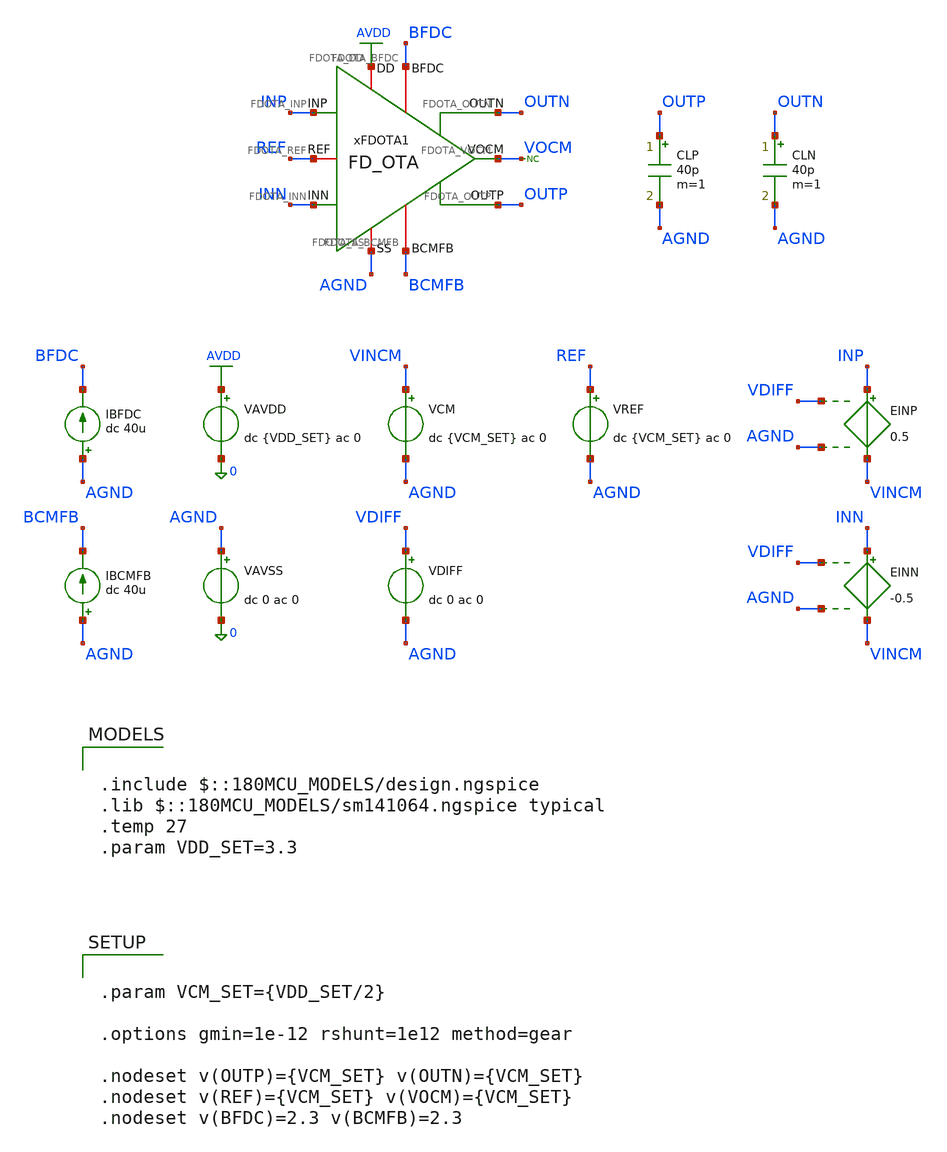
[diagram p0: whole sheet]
** sch_path: Design_Files/IC Design/Testbench/FD_OTA/FDOTA/Open_Loop/FD_OTA_TB_OL_NOM.sch
**.subckt FD_OTA_TB_OL_NOM
IBFDC AGND BFDC dc 40u
VAVDD AVDD 0 dc {VDD_SET} ac 0
.save i(vavdd)
VCM VINCM AGND dc {VCM_SET} ac 0
VDIFF VDIFF AGND dc 0 ac 0
VAVSS AGND 0 dc 0 ac 0
.save i(vavss)
VREF REF AGND dc {VCM_SET} ac 0
EINP INP VINCM VDIFF AGND 0.5
EINN INN VINCM VDIFF AGND -0.5
IBCMFB AGND BCMFB dc 40u
CLP OUTP AGND 40p m=1
CLN OUTN AGND 40p m=1
* noconn VOCM
xFDOTA1 AVDD AGND INP INN OUTN BFDC OUTP BCMFB REF VOCM FD_OTA
**** begin user architecture code

.include $::180MCU_MODELS/design.ngspice
.lib $::180MCU_MODELS/sm141064.ngspice typical
.temp 27
.param VDD_SET=3.3




.control
destroy all
save all
set wr_vecnames
set wr_singlescale
option numdgt=15

shell mkdir -p
+ /foss/designs/ECG_Acquisition_IC/Measurement_Results/IC_Simulation/FD_OTA/FDOTA/NOM.Result_txt

shell rm -f
+ /foss/designs/ECG_Acquisition_IC/Measurement_Results/IC_Simulation/FD_OTA/FDOTA/NOM.Result_txt/NOM.ol_op.txt
shell rm -f
+ /foss/designs/ECG_Acquisition_IC/Measurement_Results/IC_Simulation/FD_OTA/FDOTA/NOM.Result_txt/NOM.ol_diff_ac.txt
shell rm -f
+ /foss/designs/ECG_Acquisition_IC/Measurement_Results/IC_Simulation/FD_OTA/FDOTA/NOM.Result_txt/NOM.ol_cm_ac.txt
shell rm -f
+ /foss/designs/ECG_Acquisition_IC/Measurement_Results/IC_Simulation/FD_OTA/FDOTA/NOM.Result_txt/NOM.ol_psrrp_ac.txt
shell rm -f
+ /foss/designs/ECG_Acquisition_IC/Measurement_Results/IC_Simulation/FD_OTA/FDOTA/NOM.Result_txt/NOM.ol_psrrn_ac.txt
shell rm -f
+ /foss/designs/ECG_Acquisition_IC/Measurement_Results/IC_Simulation/FD_OTA/FDOTA/NOM.Result_txt/NOM.ol_vtc.txt

* OP
op

let voutcm = 0.5*(v(OUTP)+v(OUTN))
let voutdiff = v(OUTP)-v(OUTN)
let idd = -vavdd#branch
let ibias_fdc = 40u + 0*v(AVDD)
let ibias_cmfb = 40u + 0*v(AVDD)

wrdata
+ /foss/designs/ECG_Acquisition_IC/Measurement_Results/IC_Simulation/FD_OTA/FDOTA/NOM.Result_txt/NOM.ol_op.txt v(AVDD) v(INP) v(INN) v(OUTP) v(OUTN) voutcm voutdiff v(REF) v(VOCM) v(BFDC) v(BCMFB) idd ibias_fdc
+ ibias_cmfb

* Diff AC
alter @VCM[ACMAG] = 0
alter @VDIFF[ACMAG] = 1
alter @VDIFF[ACPHASE] = 0
alter @VREF[ACMAG] = 0
alter @VAVDD[ACMAG] = 0
alter @VAVSS[ACMAG] = 0

ac dec 200 0.01 100G

let vin_diff = v(INP)-v(INN)
let voutdiff = v(OUTP)-v(OUTN)
let vin_diff_real = real(vin_diff)
let vin_diff_imag = imag(vin_diff)
let voutdiff_real = real(voutdiff)
let voutdiff_imag = imag(voutdiff)

setscale frequency

wrdata
+ /foss/designs/ECG_Acquisition_IC/Measurement_Results/IC_Simulation/FD_OTA/FDOTA/NOM.Result_txt/NOM.ol_diff_ac.txt vin_diff_real vin_diff_imag voutdiff_real voutdiff_imag

* CM AC
alter @VCM[ACMAG] = 1
alter @VCM[ACPHASE] = 0
alter @VDIFF[ACMAG] = 0
alter @VREF[ACMAG] = 0
alter @VAVDD[ACMAG] = 0
alter @VAVSS[ACMAG] = 0

ac dec 200 0.01 100G

let vin_cm = 0.5*(v(INP)+v(INN))
let voutdiff = v(OUTP)-v(OUTN)
let vin_cm_real = real(vin_cm)
let vin_cm_imag = imag(vin_cm)
let voutdiff_real = real(voutdiff)
let voutdiff_imag = imag(voutdiff)

setscale frequency

wrdata
+ /foss/designs/ECG_Acquisition_IC/Measurement_Results/IC_Simulation/FD_OTA/FDOTA/NOM.Result_txt/NOM.ol_cm_ac.txt vin_cm_real vin_cm_imag voutdiff_real voutdiff_imag

* PSRR+
alter @VCM[ACMAG] = 0
alter @VDIFF[ACMAG] = 0
alter @VREF[ACMAG] = 0
alter @VAVDD[ACMAG] = 1
alter @VAVDD[ACPHASE] = 0
alter @VAVSS[ACMAG] = 0

ac dec 200 0.01 100G

let vavdd_ac = v(AVDD)
let voutdiff = v(OUTP)-v(OUTN)
let vavdd_real = real(vavdd_ac)
let vavdd_imag = imag(vavdd_ac)
let voutdiff_real = real(voutdiff)
let voutdiff_imag = imag(voutdiff)

setscale frequency

wrdata
+ /foss/designs/ECG_Acquisition_IC/Measurement_Results/IC_Simulation/FD_OTA/FDOTA/NOM.Result_txt/NOM.ol_psrrp_ac.txt vavdd_real vavdd_imag voutdiff_real voutdiff_imag

* PSRR-
alter @VCM[ACMAG] = 0
alter @VDIFF[ACMAG] = 0
alter @VREF[ACMAG] = 0
alter @VAVDD[ACMAG] = 0
alter @VAVSS[ACMAG] = 1
alter @VAVSS[ACPHASE] = 0

ac dec 200 0.01 100G

let vagnd_ac = v(AGND)
let voutdiff = v(OUTP)-v(OUTN)
let vagnd_real = real(vagnd_ac)
let vagnd_imag = imag(vagnd_ac)
let voutdiff_real = real(voutdiff)
let voutdiff_imag = imag(voutdiff)

setscale frequency

wrdata
+ /foss/designs/ECG_Acquisition_IC/Measurement_Results/IC_Simulation/FD_OTA/FDOTA/NOM.Result_txt/NOM.ol_psrrn_ac.txt vagnd_real vagnd_imag voutdiff_real voutdiff_imag

* VTC
alter @VCM[ACMAG] = 0
alter @VDIFF[ACMAG] = 0
alter @VREF[ACMAG] = 0
alter @VAVDD[ACMAG] = 0
alter @VAVSS[ACMAG] = 0

dc VDIFF -20m 20m 10u

let vin_diff = v(INP)-v(INN)
let voutcm = 0.5*(v(OUTP)+v(OUTN))
let voutdiff = v(OUTP)-v(OUTN)
let idd = -vavdd#branch

setscale vin_diff

wrdata
+ /foss/designs/ECG_Acquisition_IC/Measurement_Results/IC_Simulation/FD_OTA/FDOTA/NOM.Result_txt/NOM.ol_vtc.txt v(INP) v(INN) v(OUTP) v(OUTN) voutcm voutdiff v(VOCM) idd

quit
.endc




.param VCM_SET={VDD_SET/2}

.options gmin=1e-12 rshunt=1e12 method=gear

.nodeset v(OUTP)={VCM_SET} v(OUTN)={VCM_SET}
.nodeset v(REF)={VCM_SET} v(VOCM)={VCM_SET}
.nodeset v(BFDC)=2.3 v(BCMFB)=2.3


**** end user architecture code
**.ends

* expanding   symbol:  ECG_Acquisition_IC/Design_Files/IC Design/Schematic/FD_OTA/FDOTA/FD_OTA.sym #
*+ of pins=10
** sym_path: Design_Files/IC Design/Schematic/FD_OTA/FDOTA/FD_OTA.sym
** sch_path: Design_Files/IC Design/Schematic/FD_OTA/FDOTA/FD_OTA.sch
.subckt FD_OTA FDOTA_DD FDOTA_SS FDOTA_INP FDOTA_INN FDOTA_OUTN FDOTA_BFDC FDOTA_OUTP FDOTA_BCMFB
+ FDOTA_REF FDOTA_VOCM
*.iopin FDOTA_DD
*.iopin FDOTA_SS
*.ipin FDOTA_INP
*.ipin FDOTA_INN
*.opin FDOTA_OUTP
*.iopin FDOTA_BFDC
*.opin FDOTA_OUTN
*.iopin FDOTA_BCMFB
*.iopin FDOTA_REF
*.iopin FDOTA_VOCM
R1 FDOTA_OUTP FDOTA_VOCM 100k m=1
R2 FDOTA_VOCM FDOTA_OUTN 100k m=1
C1 FDOTA_OUTP FDOTA_VOCM 50f m=1
C2 FDOTA_VOCM FDOTA_OUTN 50f m=1
xFDC1 FDOTA_DD FDOTA_SS FDOTA_INP FDOTA_INN FDOTA_OUTN FDOTA_BFDC FDOTA_OUTP FDOTA_VCMFB FDC
xCMFB1 FDOTA_DD FDOTA_SS FDOTA_VOCM FDOTA_REF FDOTA_VCMFB FDOTA_BCMFB CMFB
.ends


* expanding   symbol:  ECG_Acquisition_IC/Design_Files/IC Design/Schematic/FD_OTA/FDC/FDC.sym # of
*+ pins=8
** sym_path: Design_Files/IC Design/Schematic/FD_OTA/FDC/FDC.sym
** sch_path: Design_Files/IC Design/Schematic/FD_OTA/FDC/FDC.sch
.subckt FDC FDC_DD FDC_SS FDC_INP FDC_INN FDC_OUTN FDC_B FDC_OUTP FDC_CMFB
*.iopin FDC_DD
*.iopin FDC_SS
*.ipin FDC_INP
*.ipin FDC_INN
*.opin FDC_OUTP
*.iopin FDC_B
*.opin FDC_OUTN
*.iopin FDC_CMFB
XM3 net4 FDC_CMFB FDC_DD FDC_DD pfet_03v3 L=2u W=1u nf=1 ad='int((nf+1)/2) * W/nf * 0.18u' as='int((nf+2)/2) * W/nf * 0.18u'
+ pd='2*int((nf+1)/2) * (W/nf + 0.18u)' ps='2*int((nf+2)/2) * (W/nf + 0.18u)' nrd='0.18u / W' nrs='0.18u / W'
+ sa=0 sb=0 sd=0 m=200
XM8 FDC_OUTP FDC_B FDC_SS FDC_SS nfet_03v3 L=1u W=1u nf=1 ad='int((nf+1)/2) * W/nf * 0.18u' as='int((nf+2)/2) * W/nf * 0.18u'
+ pd='2*int((nf+1)/2) * (W/nf + 0.18u)' ps='2*int((nf+2)/2) * (W/nf + 0.18u)' nrd='0.18u / W' nrs='0.18u / W'
+ sa=0 sb=0 sd=0 m=200
Rz net1 net2 6k m=1
XM5 net3 FDC_B FDC_SS FDC_SS nfet_03v3 L=2u W=1u nf=1 ad='int((nf+1)/2) * W/nf * 0.18u' as='int((nf+2)/2) * W/nf * 0.18u'
+ pd='2*int((nf+1)/2) * (W/nf + 0.18u)' ps='2*int((nf+2)/2) * (W/nf + 0.18u)' nrd='0.18u / W' nrs='0.18u / W'
+ sa=0 sb=0 sd=0 m=10
XM6 FDC_OUTP net1 FDC_DD FDC_DD pfet_03v3 L=1u W=1u nf=1 ad='int((nf+1)/2) * W/nf * 0.18u' as='int((nf+2)/2) * W/nf * 0.18u'
+ pd='2*int((nf+1)/2) * (W/nf + 0.18u)' ps='2*int((nf+2)/2) * (W/nf + 0.18u)' nrd='0.18u / W' nrs='0.18u / W'
+ sa=0 sb=0 sd=0 m=200
XM10 FDC_B FDC_B FDC_SS FDC_SS nfet_03v3 L=2u W=1u nf=1 ad='int((nf+1)/2) * W/nf * 0.18u' as='int((nf+2)/2) * W/nf * 0.18u'
+ pd='2*int((nf+1)/2) * (W/nf + 0.18u)' ps='2*int((nf+2)/2) * (W/nf + 0.18u)' nrd='0.18u / W' nrs='0.18u / W'
+ sa=0 sb=0 sd=0 m=20
Cc net2 FDC_OUTP 3p m=1
XM9 FDC_OUTN FDC_B FDC_SS FDC_SS nfet_03v3 L=1u W=1u nf=1 ad='int((nf+1)/2) * W/nf * 0.18u' as='int((nf+2)/2) * W/nf * 0.18u'
+ pd='2*int((nf+1)/2) * (W/nf + 0.18u)' ps='2*int((nf+2)/2) * (W/nf + 0.18u)' nrd='0.18u / W' nrs='0.18u / W'
+ sa=0 sb=0 sd=0 m=200
Rz1 net4 net5 6k m=1
XM7 FDC_OUTN net4 FDC_DD FDC_DD pfet_03v3 L=1u W=1u nf=1 ad='int((nf+1)/2) * W/nf * 0.18u' as='int((nf+2)/2) * W/nf * 0.18u'
+ pd='2*int((nf+1)/2) * (W/nf + 0.18u)' ps='2*int((nf+2)/2) * (W/nf + 0.18u)' nrd='0.18u / W' nrs='0.18u / W'
+ sa=0 sb=0 sd=0 m=200
Cc1 net5 FDC_OUTN 3p m=1
XM4 net1 FDC_CMFB FDC_DD FDC_DD pfet_03v3 L=2u W=1u nf=1 ad='int((nf+1)/2) * W/nf * 0.18u' as='int((nf+2)/2) * W/nf * 0.18u'
+ pd='2*int((nf+1)/2) * (W/nf + 0.18u)' ps='2*int((nf+2)/2) * (W/nf + 0.18u)' nrd='0.18u / W' nrs='0.18u / W'
+ sa=0 sb=0 sd=0 m=200
XM1 net4 FDC_INN net3 FDC_SS nfet_03v3 L=2u W=1u nf=1 ad='int((nf+1)/2) * W/nf * 0.18u' as='int((nf+2)/2) * W/nf * 0.18u'
+ pd='2*int((nf+1)/2) * (W/nf + 0.18u)' ps='2*int((nf+2)/2) * (W/nf + 0.18u)' nrd='0.18u / W' nrs='0.18u / W'
+ sa=0 sb=0 sd=0 m=200
XM2 net1 FDC_INP net3 FDC_SS nfet_03v3 L=2u W=1u nf=1 ad='int((nf+1)/2) * W/nf * 0.18u' as='int((nf+2)/2) * W/nf * 0.18u'
+ pd='2*int((nf+1)/2) * (W/nf + 0.18u)' ps='2*int((nf+2)/2) * (W/nf + 0.18u)' nrd='0.18u / W' nrs='0.18u / W'
+ sa=0 sb=0 sd=0 m=200
.ends


* expanding   symbol:  ECG_Acquisition_IC/Design_Files/IC Design/Schematic/FD_OTA/CMFB/CMFB.sym # of
*+ pins=6
** sym_path: Design_Files/IC Design/Schematic/FD_OTA/CMFB/CMFB.sym
** sch_path: Design_Files/IC Design/Schematic/FD_OTA/CMFB/CMFB.sch
.subckt CMFB CMFB_DD CMFB_SS CMFB_IN CMFB_REF CMFB_OUT CMFB_B
*.iopin CMFB_DD
*.iopin CMFB_SS
*.ipin CMFB_IN
*.ipin CMFB_REF
*.opin CMFB_OUT
*.iopin CMFB_B
XM4 CMFB_OUT CMFB_OUT CMFB_DD CMFB_DD pfet_03v3 L=1u W=1u nf=1 ad='int((nf+1)/2) * W/nf * 0.18u' as='int((nf+2)/2) * W/nf * 0.18u'
+ pd='2*int((nf+1)/2) * (W/nf + 0.18u)' ps='2*int((nf+2)/2) * (W/nf + 0.18u)' nrd='0.18u / W' nrs='0.18u / W'
+ sa=0 sb=0 sd=0 m=19
XM3 net2 net2 CMFB_DD CMFB_DD pfet_03v3 L=1u W=1u nf=1 ad='int((nf+1)/2) * W/nf * 0.18u' as='int((nf+2)/2) * W/nf * 0.18u'
+ pd='2*int((nf+1)/2) * (W/nf + 0.18u)' ps='2*int((nf+2)/2) * (W/nf + 0.18u)' nrd='0.18u / W' nrs='0.18u / W'
+ sa=0 sb=0 sd=0 m=19
XM1 net2 CMFB_REF net1 CMFB_SS nfet_03v3 L=1u W=1u nf=1 ad='int((nf+1)/2) * W/nf * 0.18u' as='int((nf+2)/2) * W/nf * 0.18u'
+ pd='2*int((nf+1)/2) * (W/nf + 0.18u)' ps='2*int((nf+2)/2) * (W/nf + 0.18u)' nrd='0.18u / W' nrs='0.18u / W'
+ sa=0 sb=0 sd=0 m=30
XM2 CMFB_OUT CMFB_IN net1 CMFB_SS nfet_03v3 L=1u W=1u nf=1 ad='int((nf+1)/2) * W/nf * 0.18u' as='int((nf+2)/2) * W/nf * 0.18u'
+ pd='2*int((nf+1)/2) * (W/nf + 0.18u)' ps='2*int((nf+2)/2) * (W/nf + 0.18u)' nrd='0.18u / W' nrs='0.18u / W'
+ sa=0 sb=0 sd=0 m=30
XM5 net1 CMFB_B CMFB_SS CMFB_SS nfet_03v3 L=2u W=1u nf=1 ad='int((nf+1)/2) * W/nf * 0.18u' as='int((nf+2)/2) * W/nf * 0.18u'
+ pd='2*int((nf+1)/2) * (W/nf + 0.18u)' ps='2*int((nf+2)/2) * (W/nf + 0.18u)' nrd='0.18u / W' nrs='0.18u / W'
+ sa=0 sb=0 sd=0 m=1
XM10 CMFB_B CMFB_B CMFB_SS CMFB_SS nfet_03v3 L=2u W=1u nf=1 ad='int((nf+1)/2) * W/nf * 0.18u' as='int((nf+2)/2) * W/nf * 0.18u'
+ pd='2*int((nf+1)/2) * (W/nf + 0.18u)' ps='2*int((nf+2)/2) * (W/nf + 0.18u)' nrd='0.18u / W' nrs='0.18u / W'
+ sa=0 sb=0 sd=0 m=10
.ends

.GLOBAL AVDD
.end
